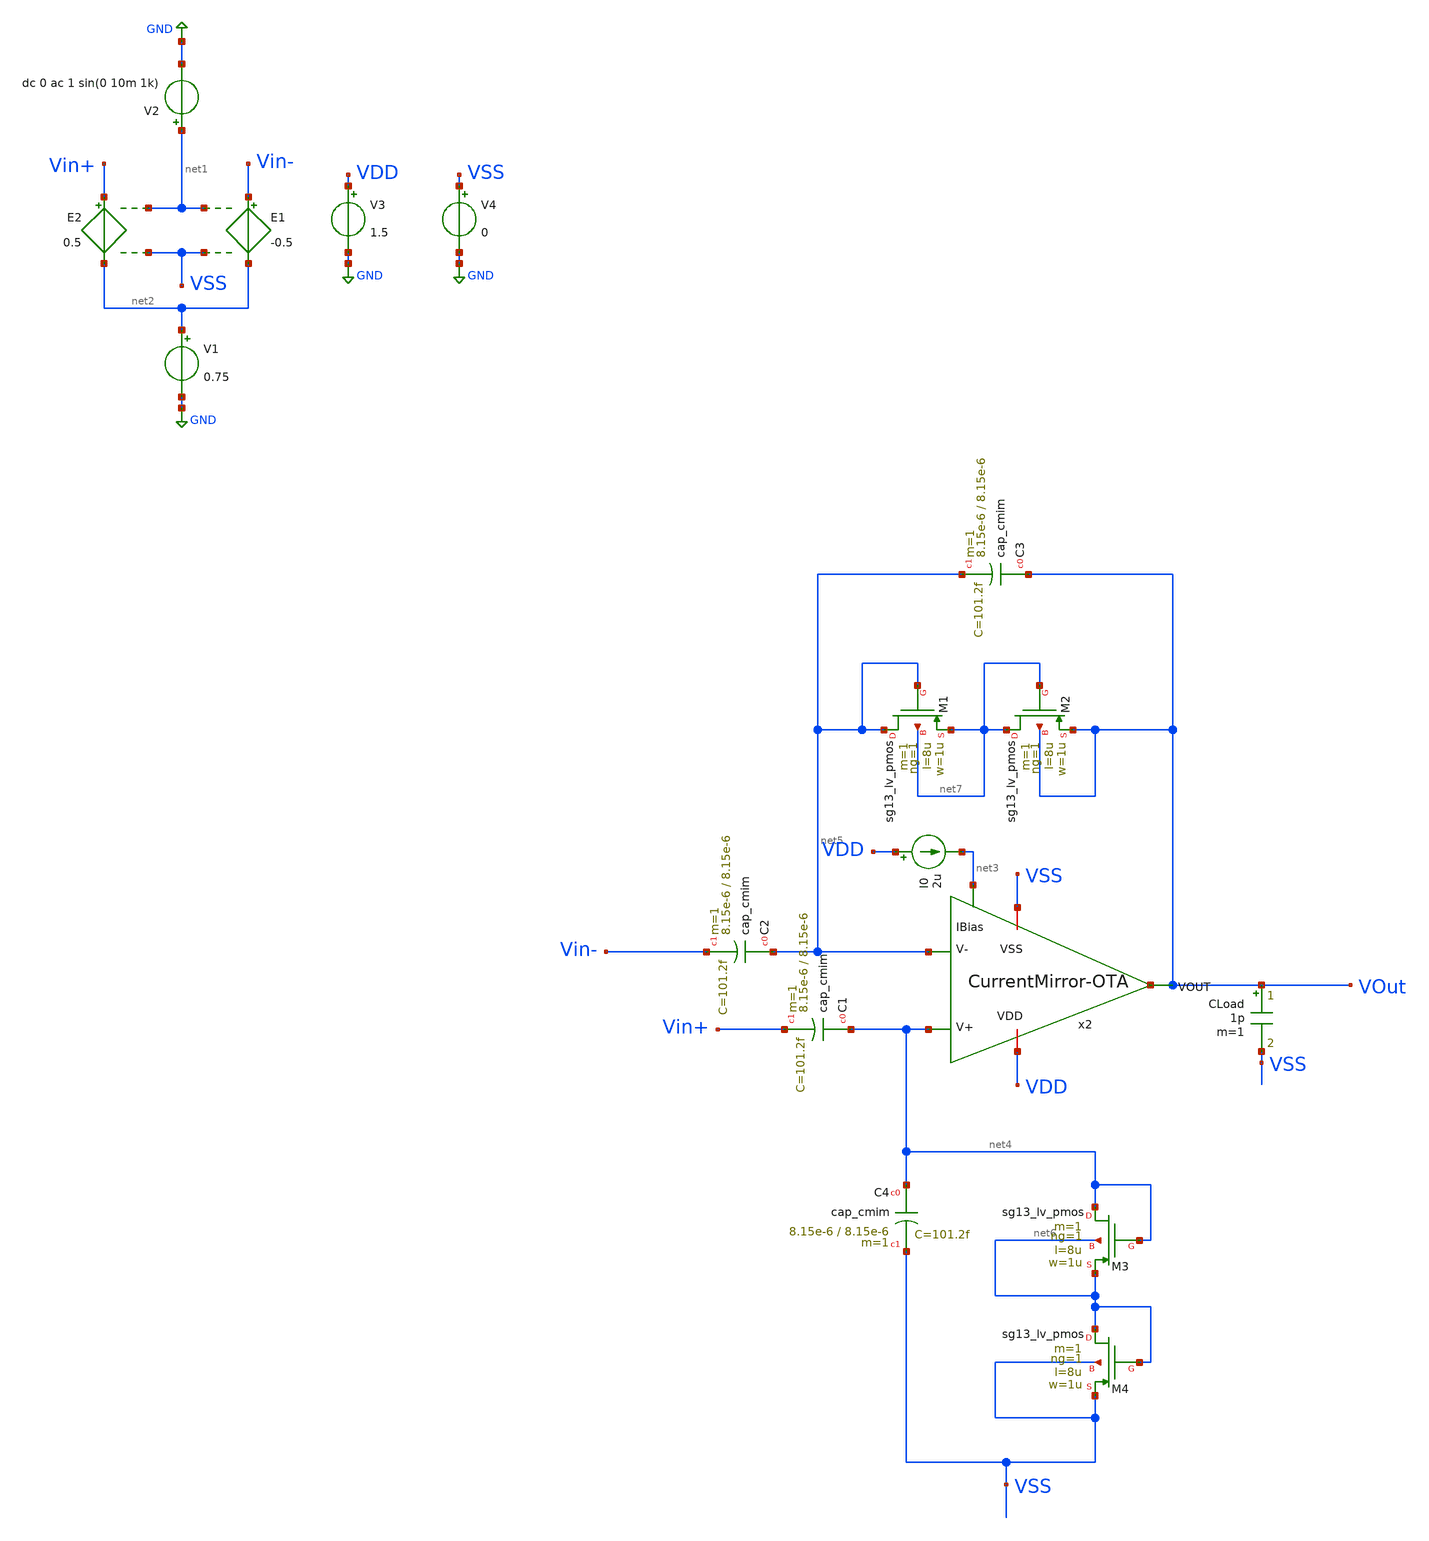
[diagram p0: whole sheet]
** sch_path: BPF/testbench_CCL.sch
**.subckt testbench_CCL
E1 Vin- net2 net1 VSS -0.5
E2 Vin+ net2 net1 VSS 0.5
V1 net2 GND 0.75
V2 net1 GND dc 0 ac 1 sin(0 10m 1k)
V3 VDD GND 1.5
V4 VSS GND 0
I0 VDD net3 2u
CLoad VOut VSS 1p m=1
XC1 net4 Vin+ cap_cmim w=8.15e-6 l=8.15e-6 m=1 mm_ok=1
XC2 net5 Vin- cap_cmim w=8.15e-6 l=8.15e-6 m=1 mm_ok=1
XM1 net5 net5 net7 net7 sg13_lv_pmos w=1u l=8u ng=1 m=1 mm_ok=1
XC3 VOut net5 cap_cmim w=8.15e-6 l=8.15e-6 m=1 mm_ok=1
XC4 net4 VSS cap_cmim w=8.15e-6 l=8.15e-6 m=1 mm_ok=1
XM4 net6 net6 VSS VSS sg13_lv_pmos w=1u l=8u ng=1 m=1 mm_ok=1
XM2 net7 net7 VOut VOut sg13_lv_pmos w=1u l=8u ng=1 m=1 mm_ok=1
XM3 net4 net4 net6 net6 sg13_lv_pmos w=1u l=8u ng=1 m=1 mm_ok=1
x2 VDD net4 net5 net3 VOut VSS CurrentMirror-OTA
**** begin user architecture code

.lib cornerMOSlv.lib mos_tt
.lib cornerMOShv.lib mos_tt
.lib $::SG13G2_MODELS/cornerCAP.lib cap_typ



.param temp=27
.save all
  @n.xm2.nsg13_lv_pmos[ids]  @n.xm3.nsg13_lv_pmos[ids]

.control
  ac dec 20 0.1 111k
  set filetype = ascii
  set units=degrees
  write testbench_CCL.raw vdb(vout) vp(vout)
  set appendwrite
  op
  set filetype = ascii
  write testbench_CCL.raw

  * tran 0.1m 11111m
  * set filetype = ascii
  * write testbench_CCL.raw v(vin+) v(vin-) v(vout)
  * set appendwrite
  * op
  * set filetype = ascii
  * write testbench_CCL.raw

.endc


**** end user architecture code
**.ends

* expanding   symbol:  /home/designer/shared/Design/CCLNA/CurrentMirror-OTA.sym # of pins=6
** sym_path: BPF/CurrentMirror-OTA.sym
** sch_path: BPF/CurrentMirror-OTA.sch
.subckt CurrentMirror-OTA VDD V+ V- IBias VOUT VSS
*.iopin VDD
*.iopin VSS
*.ipin V-
*.opin VOUT
*.ipin V+
*.ipin IBias
XM4 net1 net1 VDD VDD sg13_lv_pmos w=4u l=1u ng=1 m=1 mm_ok=1
XM3 net4 net1 VDD VDD sg13_lv_pmos w=4u l=1u ng=1 m=3 mm_ok=1
XM5 net2 net2 VDD VDD sg13_lv_pmos w=4u l=1u ng=1 m=1 mm_ok=1
XM6 VOUT net2 VDD VDD sg13_lv_pmos w=4u l=1u ng=1 m=3 mm_ok=1
XM7 net1 V- net3 net3 sg13_lv_nmos w=8u l=1u ng=1 m=1 mm_ok=1
XM8 net2 V+ net3 net3 sg13_lv_nmos w=8u l=1u ng=1 m=1 mm_ok=1
XM9 net3 IBias VSS VSS sg13_lv_nmos w=2u l=1u ng=1 m=1 mm_ok=1
XM10 IBias IBias VSS VSS sg13_lv_nmos w=2u l=1u ng=1 m=1 mm_ok=1
XM11 net4 net4 VSS VSS sg13_lv_nmos w=3u l=1u ng=1 m=1 mm_ok=1
XM12 VOUT net4 VSS VSS sg13_lv_nmos w=3u l=1u ng=1 m=1 mm_ok=1
.ends

.GLOBAL GND
.end
